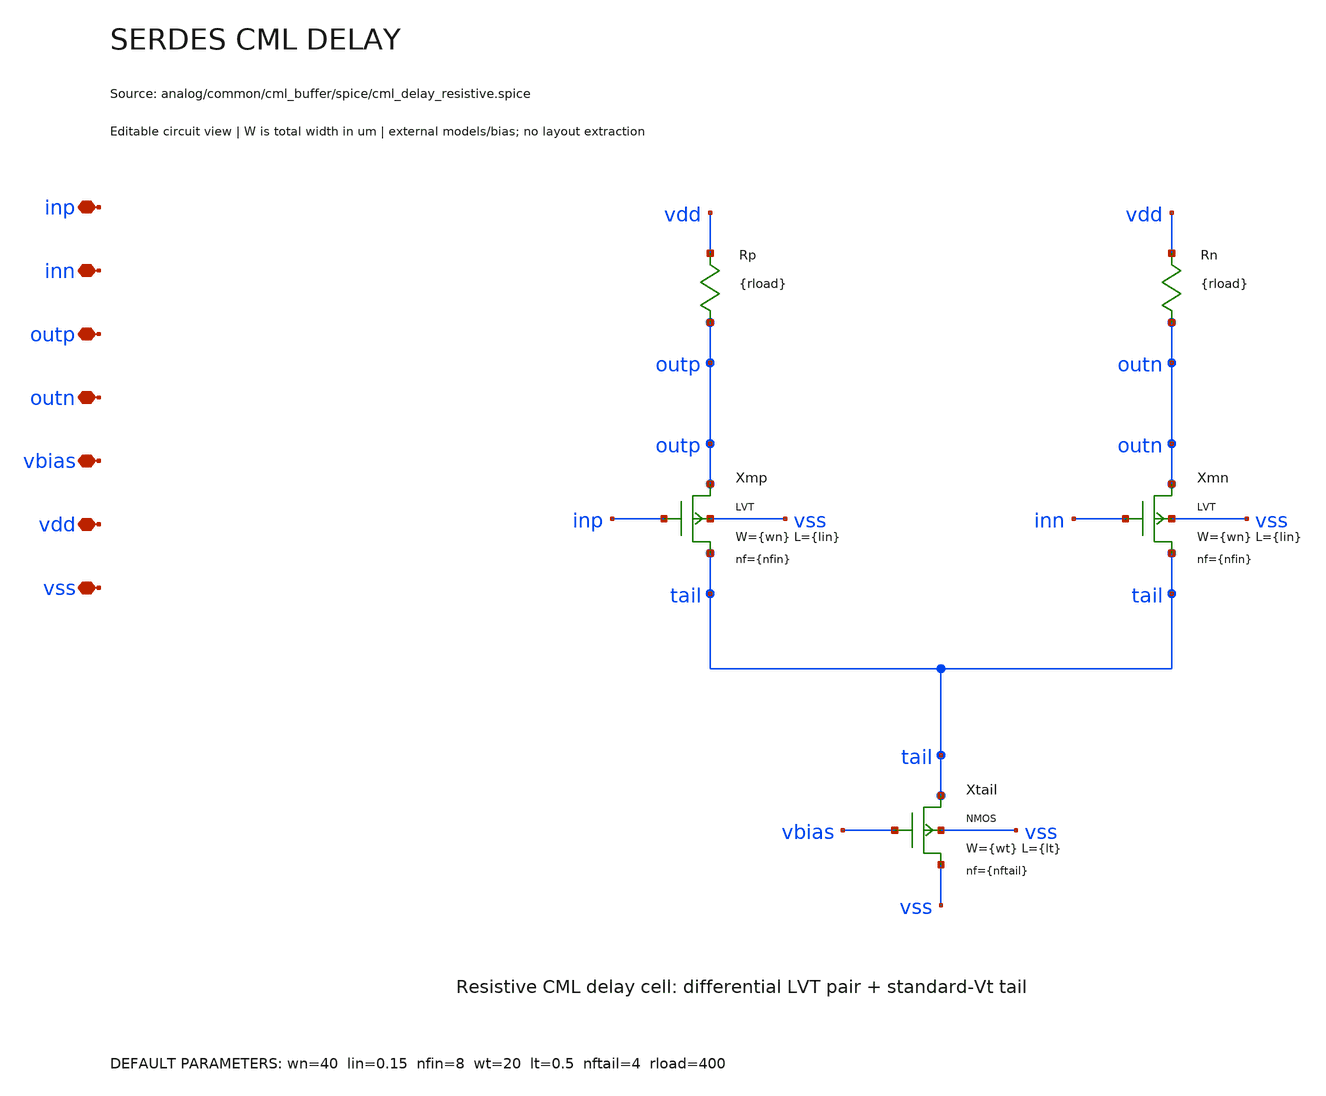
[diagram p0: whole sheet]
** sch_path: analog/common/cml_buffer/schematic/serdes_cml_delay.sch
**.subckt serdes_cml_delay inp inn outp outn vbias vdd vss
*.iopin inp
*.iopin inn
*.iopin outp
*.iopin outn
*.iopin vbias
*.iopin vdd
*.iopin vss
Rp vdd outp {rload}
Rn vdd outn {rload}
Xmp outp inp tail vss sky130_fd_pr__nfet_01v8_lvt w={wn} l={lin} nf={nfin} ad={floor((nfin+1)/2)*(wn/nfin)*0.29}
+ as={floor((nfin+2)/2)*(wn/nfin)*0.29} pd={2*floor((nfin+1)/2)*(wn/nfin+0.29)} ps={2*floor((nfin+2)/2)*(wn/nfin+0.29)}
Xmn outn inn tail vss sky130_fd_pr__nfet_01v8_lvt w={wn} l={lin} nf={nfin} ad={floor((nfin+1)/2)*(wn/nfin)*0.29}
+ as={floor((nfin+2)/2)*(wn/nfin)*0.29} pd={2*floor((nfin+1)/2)*(wn/nfin+0.29)} ps={2*floor((nfin+2)/2)*(wn/nfin+0.29)}
Xtail tail vbias vss vss sky130_fd_pr__nfet_01v8 w={wt} l={lt} nf={nftail} ad={floor((nftail+1)/2)*(wt/nftail)*0.29}
+ as={floor((nftail+2)/2)*(wt/nftail)*0.29} pd={2*floor((nftail+1)/2)*(wt/nftail+0.29)} ps={2*floor((nftail+2)/2)*(wt/nftail+0.29)}
**.ends
.end
